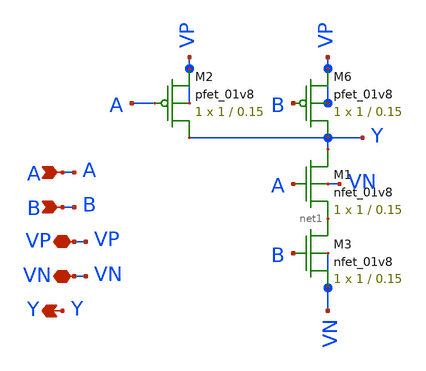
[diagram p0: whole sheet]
** sch_path: Homework1/NAND.sch
**.subckt NAND A VP B VN Y
*.ipin A
*.iopin VP
*.ipin B
*.iopin VN
*.opin Y
XM1 Y A net1 VN sky130_fd_pr__nfet_01v8 L=0.15 W=1 nf=1 ad='int((nf+1)/2) * W/nf * 0.29' as='int((nf+2)/2) * W/nf * 0.29'
+ pd='2*int((nf+1)/2) * (W/nf + 0.29)' ps='2*int((nf+2)/2) * (W/nf + 0.29)' nrd='0.29 / W' nrs='0.29 / W'
+ sa=0 sb=0 sd=0 mult=1 m=1
XM2 Y A VP VP sky130_fd_pr__pfet_01v8 L=0.15 W=1 nf=1 ad='int((nf+1)/2) * W/nf * 0.29' as='int((nf+2)/2) * W/nf * 0.29'
+ pd='2*int((nf+1)/2) * (W/nf + 0.29)' ps='2*int((nf+2)/2) * (W/nf + 0.29)' nrd='0.29 / W' nrs='0.29 / W'
+ sa=0 sb=0 sd=0 mult=1 m=1
XM6 Y B VP VP sky130_fd_pr__pfet_01v8 L=0.15 W=1 nf=1 ad='int((nf+1)/2) * W/nf * 0.29' as='int((nf+2)/2) * W/nf * 0.29'
+ pd='2*int((nf+1)/2) * (W/nf + 0.29)' ps='2*int((nf+2)/2) * (W/nf + 0.29)' nrd='0.29 / W' nrs='0.29 / W'
+ sa=0 sb=0 sd=0 mult=1 m=1
XM3 net1 B VN VN sky130_fd_pr__nfet_01v8 L=0.15 W=1 nf=1 ad='int((nf+1)/2) * W/nf * 0.29' as='int((nf+2)/2) * W/nf * 0.29'
+ pd='2*int((nf+1)/2) * (W/nf + 0.29)' ps='2*int((nf+2)/2) * (W/nf + 0.29)' nrd='0.29 / W' nrs='0.29 / W'
+ sa=0 sb=0 sd=0 mult=1 m=1
**.ends
.end
